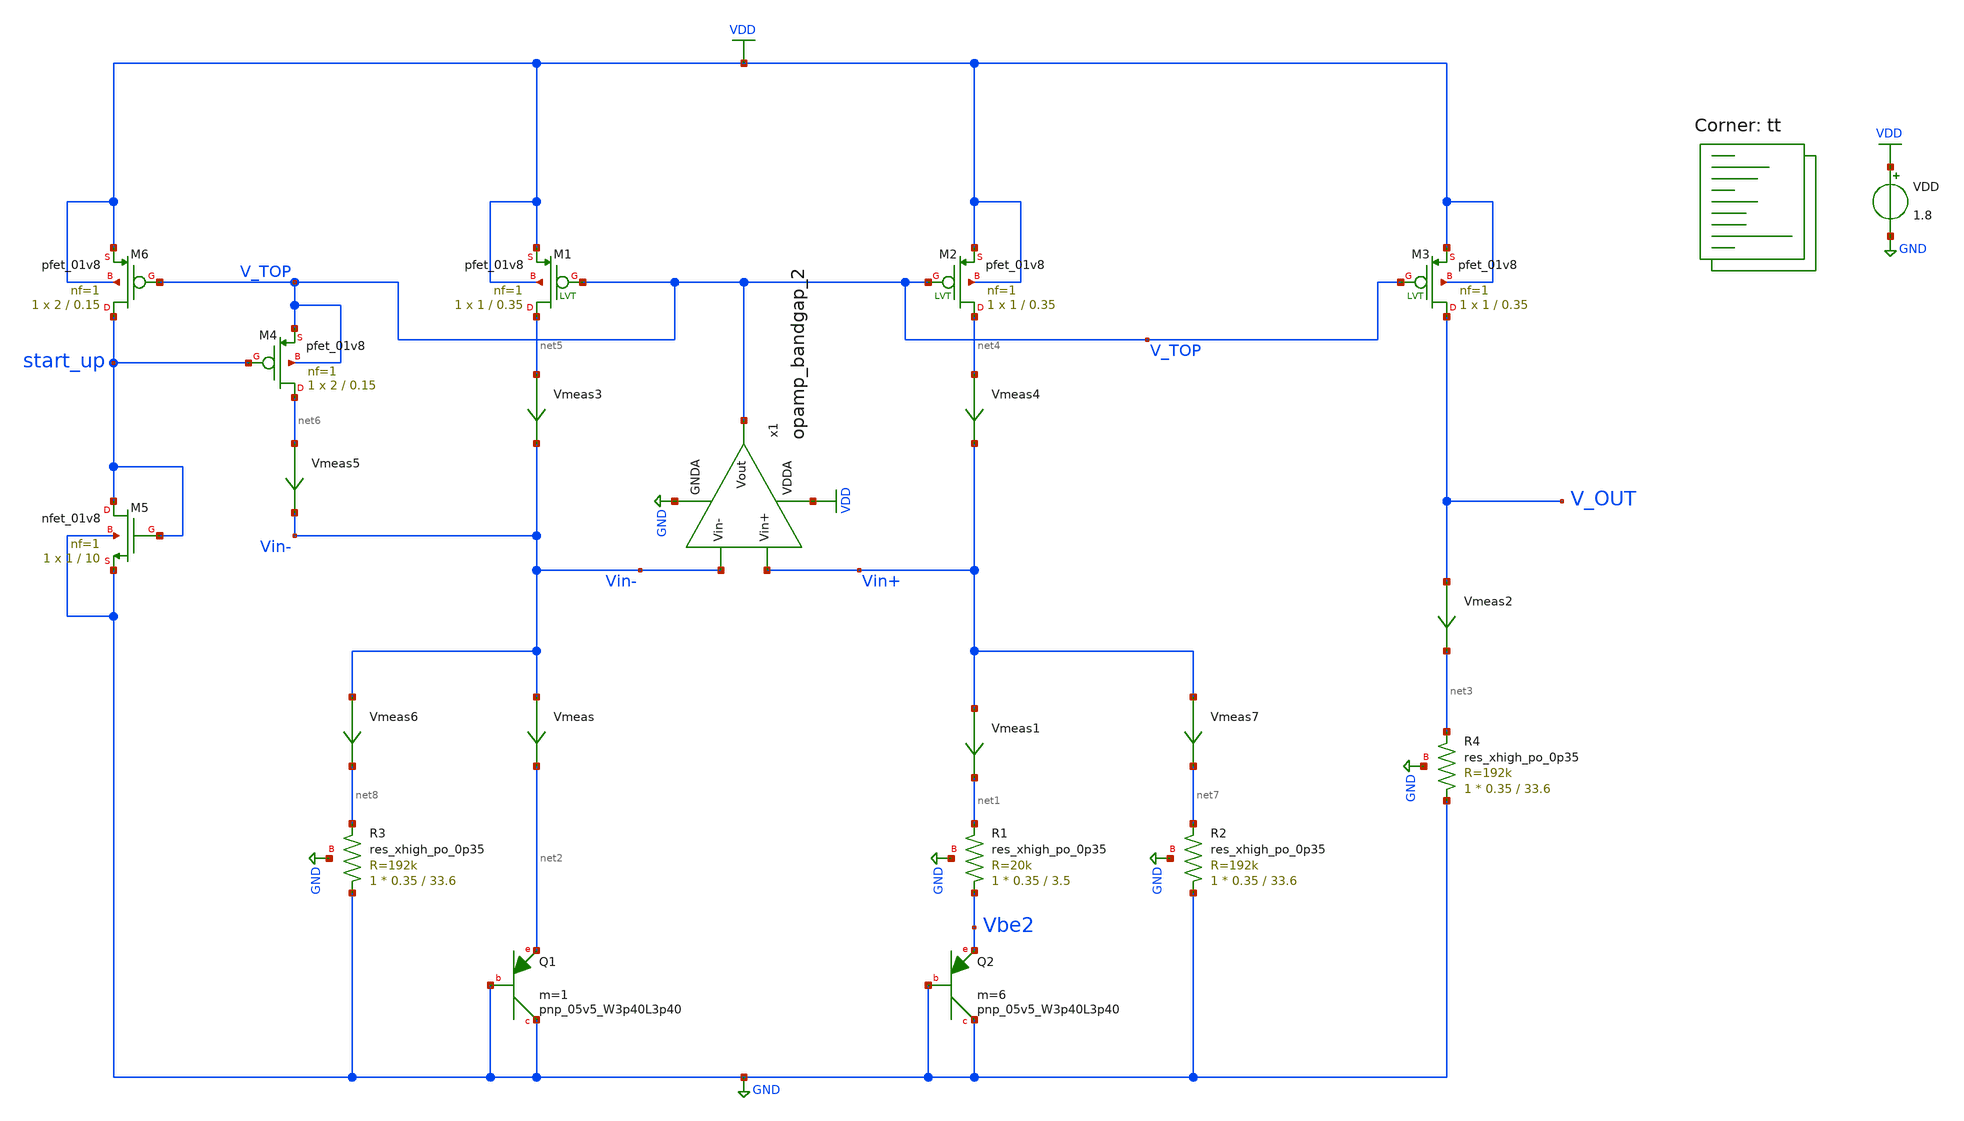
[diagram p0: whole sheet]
** sch_path: projects/bandgapref/xschem_ngspice/new_files/tb_low_voltage_BGR_lvt.sch
**.subckt tb_low_voltage_BGR_lvt
VDD VDD GND 1.8
XQ1 GND GND net2 sky130_fd_pr__pnp_05v5_W3p40L3p40 m=1
XQ2 GND GND Vbe2 sky130_fd_pr__pnp_05v5_W3p40L3p40 m=6
XM1 net5 V_TOP VDD VDD sky130_fd_pr__pfet_01v8 L=0.35 W=1 nf=1 ad='int((nf+1)/2) * W/nf * 0.29' as='int((nf+2)/2) * W/nf * 0.29'
+ pd='2*int((nf+1)/2) * (W/nf + 0.29)' ps='2*int((nf+2)/2) * (W/nf + 0.29)' nrd='0.29 / W' nrs='0.29 / W'
+ sa=0 sb=0 sd=0 mult=1 m=1
XM2 net4 V_TOP VDD VDD sky130_fd_pr__pfet_01v8 L=0.35 W=1 nf=1 ad='int((nf+1)/2) * W/nf * 0.29' as='int((nf+2)/2) * W/nf * 0.29'
+ pd='2*int((nf+1)/2) * (W/nf + 0.29)' ps='2*int((nf+2)/2) * (W/nf + 0.29)' nrd='0.29 / W' nrs='0.29 / W'
+ sa=0 sb=0 sd=0 mult=1 m=1
XM3 V_OUT V_TOP VDD VDD sky130_fd_pr__pfet_01v8 L=0.35 W=1 nf=1 ad='int((nf+1)/2) * W/nf * 0.29' as='int((nf+2)/2) * W/nf * 0.29'
+ pd='2*int((nf+1)/2) * (W/nf + 0.29)' ps='2*int((nf+2)/2) * (W/nf + 0.29)' nrd='0.29 / W' nrs='0.29 / W'
+ sa=0 sb=0 sd=0 mult=1 m=1
Vmeas Vin- net2 0
.save i(vmeas)
Vmeas1 Vin+ net1 0
.save i(vmeas1)
Vmeas2 V_OUT net3 0
.save i(vmeas2)
XR1 Vbe2 net1 GND sky130_fd_pr__res_xhigh_po_0p35 L=3.5 mult=1 m=1
XR2 GND net7 GND sky130_fd_pr__res_xhigh_po_0p35 L=33.6 mult=1 m=1
XR3 GND net8 GND sky130_fd_pr__res_xhigh_po_0p35 L=33.6 mult=1 m=1
XR4 GND net3 GND sky130_fd_pr__res_xhigh_po_0p35 L=33.6 mult=1 m=1
Vmeas3 net5 Vin- 0
.save i(vmeas3)
Vmeas4 net4 Vin+ 0
.save i(vmeas4)
x1 VDD V_TOP Vin- Vin+ GND opamp_bandgap_2
XM5 start_up start_up GND GND sky130_fd_pr__nfet_01v8 L=10 W=1 nf=1 ad='int((nf+1)/2) * W/nf * 0.29'
+ as='int((nf+2)/2) * W/nf * 0.29' pd='2*int((nf+1)/2) * (W/nf + 0.29)' ps='2*int((nf+2)/2) * (W/nf + 0.29)'
+ nrd='0.29 / W' nrs='0.29 / W' sa=0 sb=0 sd=0 mult=1 m=1
XM6 start_up V_TOP VDD VDD sky130_fd_pr__pfet_01v8 L=0.15 W=2 nf=1 ad='int((nf+1)/2) * W/nf * 0.29' as='int((nf+2)/2) * W/nf * 0.29'
+ pd='2*int((nf+1)/2) * (W/nf + 0.29)' ps='2*int((nf+2)/2) * (W/nf + 0.29)' nrd='0.29 / W' nrs='0.29 / W'
+ sa=0 sb=0 sd=0 mult=1 m=1
Vmeas5 net6 Vin- 0
.save i(vmeas5)
XM4 net6 start_up V_TOP V_TOP sky130_fd_pr__pfet_01v8 L=0.15 W=2 nf=1 ad='int((nf+1)/2) * W/nf * 0.29'
+ as='int((nf+2)/2) * W/nf * 0.29' pd='2*int((nf+1)/2) * (W/nf + 0.29)' ps='2*int((nf+2)/2) * (W/nf + 0.29)'
+ nrd='0.29 / W' nrs='0.29 / W' sa=0 sb=0 sd=0 mult=1 m=1
Vmeas6 Vin- net8 0
.save i(vmeas6)
Vmeas7 Vin+ net7 0
.save i(vmeas7)
**** begin user architecture code
.lib $::SKYWATER_MODELS/sky130.lib.spice tt



.option method=gear
.option wnflag=1
.option savecurrents
* .temp =140

.save @m.xm1.msky130_fd_pr__pfet_01v8[gm] @m.xm2.msky130_fd_pr__pfet_01v8[gm] @m.xm3.msky130_fd_pr__pfet_01v8[gm] @m.xm4.msky130_fd_pr__pfet_01v8[gm] @m.xm4.msky130_fd_pr__nfet_01v8[gm] @m.x1.xm1.msky130_fd_pr__nfet_01v8[gm] @m.x1.xm2.msky130_fd_pr__nfet_01v8[gm] @m.x1.xm3.msky130_fd_pr__nfet_01v8[gm] @m.x1.xm4.msky130_fd_pr__pfet_01v8[gm] @m.x1.xm5.msky130_fd_pr__pfet_01v8[gm] @m.x1.xm6.msky130_fd_pr__nfet_01v8[gm] @m.x1.xm7.msky130_fd_pr__pfet_01v8[gm] @m.x2.xm1.msky130_fd_pr__nfet_01v8[gm] @m.x2.xm2.msky130_fd_pr__nfet_01v8[gm] @m.x2.xm3.msky130_fd_pr__nfet_01v8[gm] @m.x2.xm4.msky130_fd_pr__pfet_01v8[gm] @m.x2.xm5.msky130_fd_pr__pfet_01v8[gm] @m.x2.xm6.msky130_fd_pr__pfet_01v8[gm] @m.x2.xm7.msky130_fd_pr__pfet_01v8[gm]

* .ic v(vin-) = 0.8
* .ic v(v_top) = 1.8

.control
  save all
  * dc temp -40 120 10 VDD 0 4.0 0.2
  dc VDD 0 2.0 0.02 temp -40 120 40
  * dc VDD 0 2.0 0.01
  * tran 1ns 10us
  remzerovec
  write tb_low_voltage_BGR_lvt.raw
  set appendwrite
.endc




**** end user architecture code
**.ends

* expanding   symbol:  opamp_bandgap_2.sym # of pins=5
** sym_path: projects/bandgapref/xschem_ngspice/new_files/opamp_bandgap_2.sym
** sch_path: projects/bandgapref/xschem_ngspice/new_files/opamp_bandgap_2.sch
.subckt opamp_bandgap_2 VDDA Vout Vin- Vin+ GNDA
*.ipin Vin+
*.opin Vout
*.ipin Vin-
*.ipin GNDA
*.ipin VDDA
XM1 V_p V_mirror GNDA GNDA sky130_fd_pr__nfet_01v8 L=10 W=10 nf=1 ad='int((nf+1)/2) * W/nf * 0.29' as='int((nf+2)/2) * W/nf * 0.29'
+ pd='2*int((nf+1)/2) * (W/nf + 0.29)' ps='2*int((nf+2)/2) * (W/nf + 0.29)' nrd='0.29 / W' nrs='0.29 / W'
+ sa=0 sb=0 sd=0 mult=1 m=1
XM2 V_mirror Vin- V_p GNDA sky130_fd_pr__nfet_01v8 L=1.2 W=10 nf=1 ad='int((nf+1)/2) * W/nf * 0.29' as='int((nf+2)/2) * W/nf * 0.29'
+ pd='2*int((nf+1)/2) * (W/nf + 0.29)' ps='2*int((nf+2)/2) * (W/nf + 0.29)' nrd='0.29 / W' nrs='0.29 / W'
+ sa=0 sb=0 sd=0 mult=1 m=1
XM3 1st_Vout Vin+ V_p GNDA sky130_fd_pr__nfet_01v8 L=1.2 W=10 nf=1 ad='int((nf+1)/2) * W/nf * 0.29' as='int((nf+2)/2) * W/nf * 0.29'
+ pd='2*int((nf+1)/2) * (W/nf + 0.29)' ps='2*int((nf+2)/2) * (W/nf + 0.29)' nrd='0.29 / W' nrs='0.29 / W'
+ sa=0 sb=0 sd=0 mult=1 m=1
XM4 V_mirror V_mirror VDDA VDDA sky130_fd_pr__pfet_01v8 L=1.2 W=20 nf=2 ad='int((nf+1)/2) * W/nf * 0.29'
+ as='int((nf+2)/2) * W/nf * 0.29' pd='2*int((nf+1)/2) * (W/nf + 0.29)' ps='2*int((nf+2)/2) * (W/nf + 0.29)'
+ nrd='0.29 / W' nrs='0.29 / W' sa=0 sb=0 sd=0 mult=1 m=1
XM5 1st_Vout V_mirror VDDA VDDA sky130_fd_pr__pfet_01v8 L=1.2 W=20 nf=2 ad='int((nf+1)/2) * W/nf * 0.29'
+ as='int((nf+2)/2) * W/nf * 0.29' pd='2*int((nf+1)/2) * (W/nf + 0.29)' ps='2*int((nf+2)/2) * (W/nf + 0.29)'
+ nrd='0.29 / W' nrs='0.29 / W' sa=0 sb=0 sd=0 mult=1 m=1
XM6 Vout V_mirror GNDA GNDA sky130_fd_pr__nfet_01v8 L=10 W=10 nf=1 ad='int((nf+1)/2) * W/nf * 0.29' as='int((nf+2)/2) * W/nf * 0.29'
+ pd='2*int((nf+1)/2) * (W/nf + 0.29)' ps='2*int((nf+2)/2) * (W/nf + 0.29)' nrd='0.29 / W' nrs='0.29 / W'
+ sa=0 sb=0 sd=0 mult=1 m=1
XM7 Vout 1st_Vout VDDA VDDA sky130_fd_pr__pfet_01v8 L=1.2 W=20 nf=2 ad='int((nf+1)/2) * W/nf * 0.29'
+ as='int((nf+2)/2) * W/nf * 0.29' pd='2*int((nf+1)/2) * (W/nf + 0.29)' ps='2*int((nf+2)/2) * (W/nf + 0.29)'
+ nrd='0.29 / W' nrs='0.29 / W' sa=0 sb=0 sd=0 mult=1 m=1
.ends

.GLOBAL GND
.GLOBAL VDD
.end
